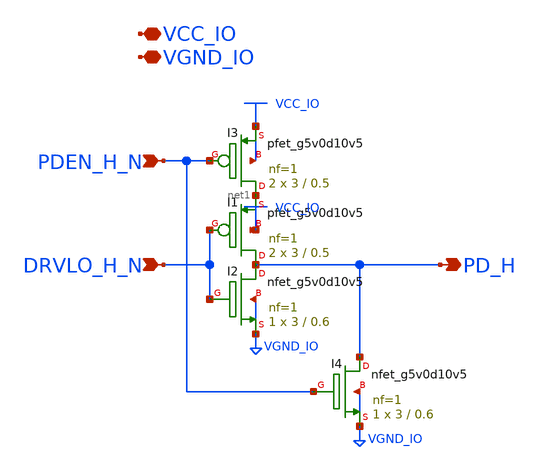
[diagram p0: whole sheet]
** sch_path: com_pdpredrvr_strong_slow.sch
* Copyright 2023 David Mitchell Bailey
* Licensed under the Apache License, Version 2.0 (the "License");
* you may not use this file except in compliance with the License.
* You may obtain a copy of the License at
* https://www.apache.org/licenses/LICENSE-2.0
* Unless required by applicable law or agreed to in writing, software
* distributed under the License is distributed on an "AS IS" BASIS,
* WITHOUT WARRANTIES OR CONDITIONS OF ANY KIND, either express or implied.
* See the License for the specific language governing permissions and
* limitations under the License.
**.subckt com_pdpredrvr_strong_slow DRVLO_H_N PD_H VCC_IO VGND_IO PDEN_H_N
*.ipin DRVLO_H_N
*.opin PD_H
*.iopin VCC_IO
*.iopin VGND_IO
*.ipin PDEN_H_N
XI2 PD_H DRVLO_H_N VGND_IO VGND_IO sky130_fd_pr__nfet_g5v0d10v5 L=0.6 W=3 nf=1 ad='int((nf+1)/2) * W/nf * 0.29'
+ as='int((nf+2)/2) * W/nf * 0.29' pd='2*int((nf+1)/2) * (W/nf + 0.29)' ps='2*int((nf+2)/2) * (W/nf + 0.29)'
+ nrd='0.29 / W' nrs='0.29 / W' sa=0 sb=0 sd=0 mult=1 m=1
XI1 PD_H DRVLO_H_N net1 VCC_IO sky130_fd_pr__pfet_g5v0d10v5 L=0.5 W=3 nf=1 ad='int((nf+1)/2) * W/nf * 0.29'
+ as='int((nf+2)/2) * W/nf * 0.29' pd='2*int((nf+1)/2) * (W/nf + 0.29)' ps='2*int((nf+2)/2) * (W/nf + 0.29)'
+ nrd='0.29 / W' nrs='0.29 / W' sa=0 sb=0 sd=0 mult=2 m=2
XI3 net1 PDEN_H_N VCC_IO VCC_IO sky130_fd_pr__pfet_g5v0d10v5 L=0.5 W=3 nf=1 ad='int((nf+1)/2) * W/nf * 0.29'
+ as='int((nf+2)/2) * W/nf * 0.29' pd='2*int((nf+1)/2) * (W/nf + 0.29)' ps='2*int((nf+2)/2) * (W/nf + 0.29)'
+ nrd='0.29 / W' nrs='0.29 / W' sa=0 sb=0 sd=0 mult=2 m=2
XI4 PD_H PDEN_H_N VGND_IO VGND_IO sky130_fd_pr__nfet_g5v0d10v5 L=0.6 W=3 nf=1 ad='int((nf+1)/2) * W/nf * 0.29'
+ as='int((nf+2)/2) * W/nf * 0.29' pd='2*int((nf+1)/2) * (W/nf + 0.29)' ps='2*int((nf+2)/2) * (W/nf + 0.29)'
+ nrd='0.29 / W' nrs='0.29 / W' sa=0 sb=0 sd=0 mult=1 m=1
**.ends
.end
